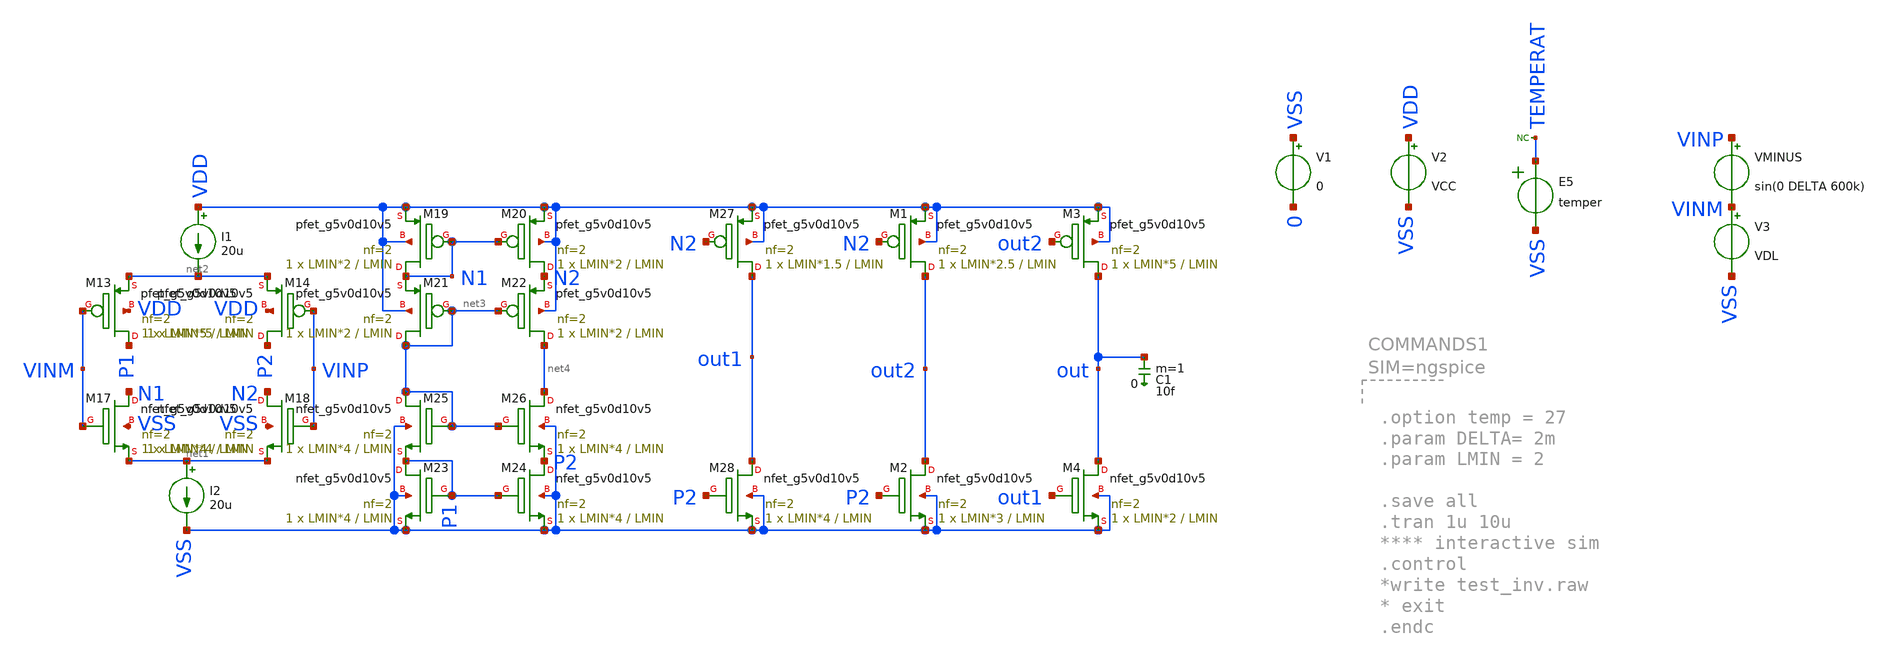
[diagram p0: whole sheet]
** sch_path: Comparator/schematic/static_good/tb_comparator.sch
.lib $::SKYWATER_MODELS/sky130.lib.spice.tt.red tt
.include $::SKYWATER_STDCELLS/sky130_fd_sc_hd.spice

**.subckt tb_comparator
V1 VSS 0 0
V2 VDD VSS VCC
VMINUS VINP VINM sin(0 DELTA 600k)
XM13 P1 VINM net2 VDD sky130_fd_pr__pfet_g5v0d10v5 L=LMIN W=LMIN*5 nf=2 ad='int((nf+1)/2) * W/nf * 0.29'
+ as='int((nf+2)/2) * W/nf * 0.29' pd='2*int((nf+1)/2) * (W/nf + 0.29)' ps='2*int((nf+2)/2) * (W/nf + 0.29)'
+ nrd='0.29 / W' nrs='0.29 / W' sa=0 sb=0 sd=0 mult=1 m=1
XM14 P2 VINP net2 VDD sky130_fd_pr__pfet_g5v0d10v5 L=LMIN W=LMIN*5 nf=2 ad='int((nf+1)/2) * W/nf * 0.29'
+ as='int((nf+2)/2) * W/nf * 0.29' pd='2*int((nf+1)/2) * (W/nf + 0.29)' ps='2*int((nf+2)/2) * (W/nf + 0.29)'
+ nrd='0.29 / W' nrs='0.29 / W' sa=0 sb=0 sd=0 mult=1 m=1
XM17 N1 VINM net1 VSS sky130_fd_pr__nfet_g5v0d10v5 L=LMIN W=LMIN*4 nf=2 ad='int((nf+1)/2) * W/nf * 0.29'
+ as='int((nf+2)/2) * W/nf * 0.29' pd='2*int((nf+1)/2) * (W/nf + 0.29)' ps='2*int((nf+2)/2) * (W/nf + 0.29)'
+ nrd='0.29 / W' nrs='0.29 / W' sa=0 sb=0 sd=0 mult=1 m=1
XM18 N2 VINP net1 VSS sky130_fd_pr__nfet_g5v0d10v5 L=LMIN W=LMIN*4 nf=2 ad='int((nf+1)/2) * W/nf * 0.29'
+ as='int((nf+2)/2) * W/nf * 0.29' pd='2*int((nf+1)/2) * (W/nf + 0.29)' ps='2*int((nf+2)/2) * (W/nf + 0.29)'
+ nrd='0.29 / W' nrs='0.29 / W' sa=0 sb=0 sd=0 mult=1 m=1
XM19 N1 N1 VDD VDD sky130_fd_pr__pfet_g5v0d10v5 L=LMIN W=LMIN*2 nf=2 ad='int((nf+1)/2) * W/nf * 0.29'
+ as='int((nf+2)/2) * W/nf * 0.29' pd='2*int((nf+1)/2) * (W/nf + 0.29)' ps='2*int((nf+2)/2) * (W/nf + 0.29)'
+ nrd='0.29 / W' nrs='0.29 / W' sa=0 sb=0 sd=0 mult=1 m=1
XM20 N2 N1 VDD VDD sky130_fd_pr__pfet_g5v0d10v5 L=LMIN W=LMIN*2 nf=2 ad='int((nf+1)/2) * W/nf * 0.29'
+ as='int((nf+2)/2) * W/nf * 0.29' pd='2*int((nf+1)/2) * (W/nf + 0.29)' ps='2*int((nf+2)/2) * (W/nf + 0.29)'
+ nrd='0.29 / W' nrs='0.29 / W' sa=0 sb=0 sd=0 mult=1 m=1
XM21 net3 net3 N1 VDD sky130_fd_pr__pfet_g5v0d10v5 L=LMIN W=LMIN*2 nf=2 ad='int((nf+1)/2) * W/nf * 0.29'
+ as='int((nf+2)/2) * W/nf * 0.29' pd='2*int((nf+1)/2) * (W/nf + 0.29)' ps='2*int((nf+2)/2) * (W/nf + 0.29)'
+ nrd='0.29 / W' nrs='0.29 / W' sa=0 sb=0 sd=0 mult=1 m=1
XM22 net4 net3 N2 VDD sky130_fd_pr__pfet_g5v0d10v5 L=LMIN W=LMIN*2 nf=2 ad='int((nf+1)/2) * W/nf * 0.29'
+ as='int((nf+2)/2) * W/nf * 0.29' pd='2*int((nf+1)/2) * (W/nf + 0.29)' ps='2*int((nf+2)/2) * (W/nf + 0.29)'
+ nrd='0.29 / W' nrs='0.29 / W' sa=0 sb=0 sd=0 mult=1 m=1
XM23 P1 P1 VSS VSS sky130_fd_pr__nfet_g5v0d10v5 L=LMIN W=LMIN*4 nf=2 ad='int((nf+1)/2) * W/nf * 0.29'
+ as='int((nf+2)/2) * W/nf * 0.29' pd='2*int((nf+1)/2) * (W/nf + 0.29)' ps='2*int((nf+2)/2) * (W/nf + 0.29)'
+ nrd='0.29 / W' nrs='0.29 / W' sa=0 sb=0 sd=0 mult=1 m=1
XM24 P2 P1 VSS VSS sky130_fd_pr__nfet_g5v0d10v5 L=LMIN W=LMIN*4 nf=2 ad='int((nf+1)/2) * W/nf * 0.29'
+ as='int((nf+2)/2) * W/nf * 0.29' pd='2*int((nf+1)/2) * (W/nf + 0.29)' ps='2*int((nf+2)/2) * (W/nf + 0.29)'
+ nrd='0.29 / W' nrs='0.29 / W' sa=0 sb=0 sd=0 mult=1 m=1
XM25 net3 net3 P1 VSS sky130_fd_pr__nfet_g5v0d10v5 L=LMIN W=LMIN*4 nf=2 ad='int((nf+1)/2) * W/nf * 0.29'
+ as='int((nf+2)/2) * W/nf * 0.29' pd='2*int((nf+1)/2) * (W/nf + 0.29)' ps='2*int((nf+2)/2) * (W/nf + 0.29)'
+ nrd='0.29 / W' nrs='0.29 / W' sa=0 sb=0 sd=0 mult=1 m=1
XM26 net4 net3 P2 VSS sky130_fd_pr__nfet_g5v0d10v5 L=LMIN W=LMIN*4 nf=2 ad='int((nf+1)/2) * W/nf * 0.29'
+ as='int((nf+2)/2) * W/nf * 0.29' pd='2*int((nf+1)/2) * (W/nf + 0.29)' ps='2*int((nf+2)/2) * (W/nf + 0.29)'
+ nrd='0.29 / W' nrs='0.29 / W' sa=0 sb=0 sd=0 mult=1 m=1
XM27 out1 N2 VDD VDD sky130_fd_pr__pfet_g5v0d10v5 L=LMIN W=LMIN*1.5 nf=2 ad='int((nf+1)/2) * W/nf * 0.29'
+ as='int((nf+2)/2) * W/nf * 0.29' pd='2*int((nf+1)/2) * (W/nf + 0.29)' ps='2*int((nf+2)/2) * (W/nf + 0.29)'
+ nrd='0.29 / W' nrs='0.29 / W' sa=0 sb=0 sd=0 mult=1 m=1
XM28 out1 P2 VSS VSS sky130_fd_pr__nfet_g5v0d10v5 L=LMIN W=LMIN*4 nf=2 ad='int((nf+1)/2) * W/nf * 0.29'
+ as='int((nf+2)/2) * W/nf * 0.29' pd='2*int((nf+1)/2) * (W/nf + 0.29)' ps='2*int((nf+2)/2) * (W/nf + 0.29)'
+ nrd='0.29 / W' nrs='0.29 / W' sa=0 sb=0 sd=0 mult=1 m=1
I1 VDD net2 20u
I2 net1 VSS 20u
V3 VINM VSS VDL
XM1 out2 N2 VDD VDD sky130_fd_pr__pfet_g5v0d10v5 L=LMIN W=LMIN*2.5 nf=2 ad='int((nf+1)/2) * W/nf * 0.29'
+ as='int((nf+2)/2) * W/nf * 0.29' pd='2*int((nf+1)/2) * (W/nf + 0.29)' ps='2*int((nf+2)/2) * (W/nf + 0.29)'
+ nrd='0.29 / W' nrs='0.29 / W' sa=0 sb=0 sd=0 mult=1 m=1
XM2 out2 P2 VSS VSS sky130_fd_pr__nfet_g5v0d10v5 L=LMIN W=LMIN*3 nf=2 ad='int((nf+1)/2) * W/nf * 0.29'
+ as='int((nf+2)/2) * W/nf * 0.29' pd='2*int((nf+1)/2) * (W/nf + 0.29)' ps='2*int((nf+2)/2) * (W/nf + 0.29)'
+ nrd='0.29 / W' nrs='0.29 / W' sa=0 sb=0 sd=0 mult=1 m=1
XM3 out out2 VDD VDD sky130_fd_pr__pfet_g5v0d10v5 L=LMIN W=LMIN*5 nf=2 ad='int((nf+1)/2) * W/nf * 0.29'
+ as='int((nf+2)/2) * W/nf * 0.29' pd='2*int((nf+1)/2) * (W/nf + 0.29)' ps='2*int((nf+2)/2) * (W/nf + 0.29)'
+ nrd='0.29 / W' nrs='0.29 / W' sa=0 sb=0 sd=0 mult=1 m=1
XM4 out out1 VSS VSS sky130_fd_pr__nfet_g5v0d10v5 L=LMIN W=LMIN*2 nf=2 ad='int((nf+1)/2) * W/nf * 0.29'
+ as='int((nf+2)/2) * W/nf * 0.29' pd='2*int((nf+1)/2) * (W/nf + 0.29)' ps='2*int((nf+2)/2) * (W/nf + 0.29)'
+ nrd='0.29 / W' nrs='0.29 / W' sa=0 sb=0 sd=0 mult=1 m=1
C1 out 0 10f m=1
E5 TEMPERAT VSS VOL=' temper '
* noconn TEMPERAT
**.ends
**** begin user architecture code


** this experimental option enables mos model bin
** selection based on W/NF instead of W
.option chgtol=4e-16 method=gear

.param VCC_VAR =10
.param VCCGAUSS = aunif(3.3, 0.033*VCC_VAR)
.param VCC = 'VCCGAUSS'
** use following line to remove VCC variations
*.param VCC = 3.3
.param VDLGAUSS = aunif(1.65, 1.65)
.param VDL = VDLGAUSS
* use following line to remove input common mode variations
*.param VDL =  0.2
.param TEMPGAUSS = agauss(40, 30, 1)
.option temp = 'TEMPGAUSS'
** use following line to remove temperature variations
*.option temp = 27
.param DELTA = 2m
.param LMIN = 2

*.option savecurrents
.control
  let mc_runs = 10
  option seed = 8
  let run = 1
  save all
  op
  write tb_comparator.raw
  reset
  set appendwrite
  dowhile run < = mc_runs
    save vinp vinm out1 out2 out vdd temperat
    tran 1u 10u
    write tb_comparator.raw
    let run = run + 1
    reset
  end

quit
.endc


**** end user architecture code
.end
